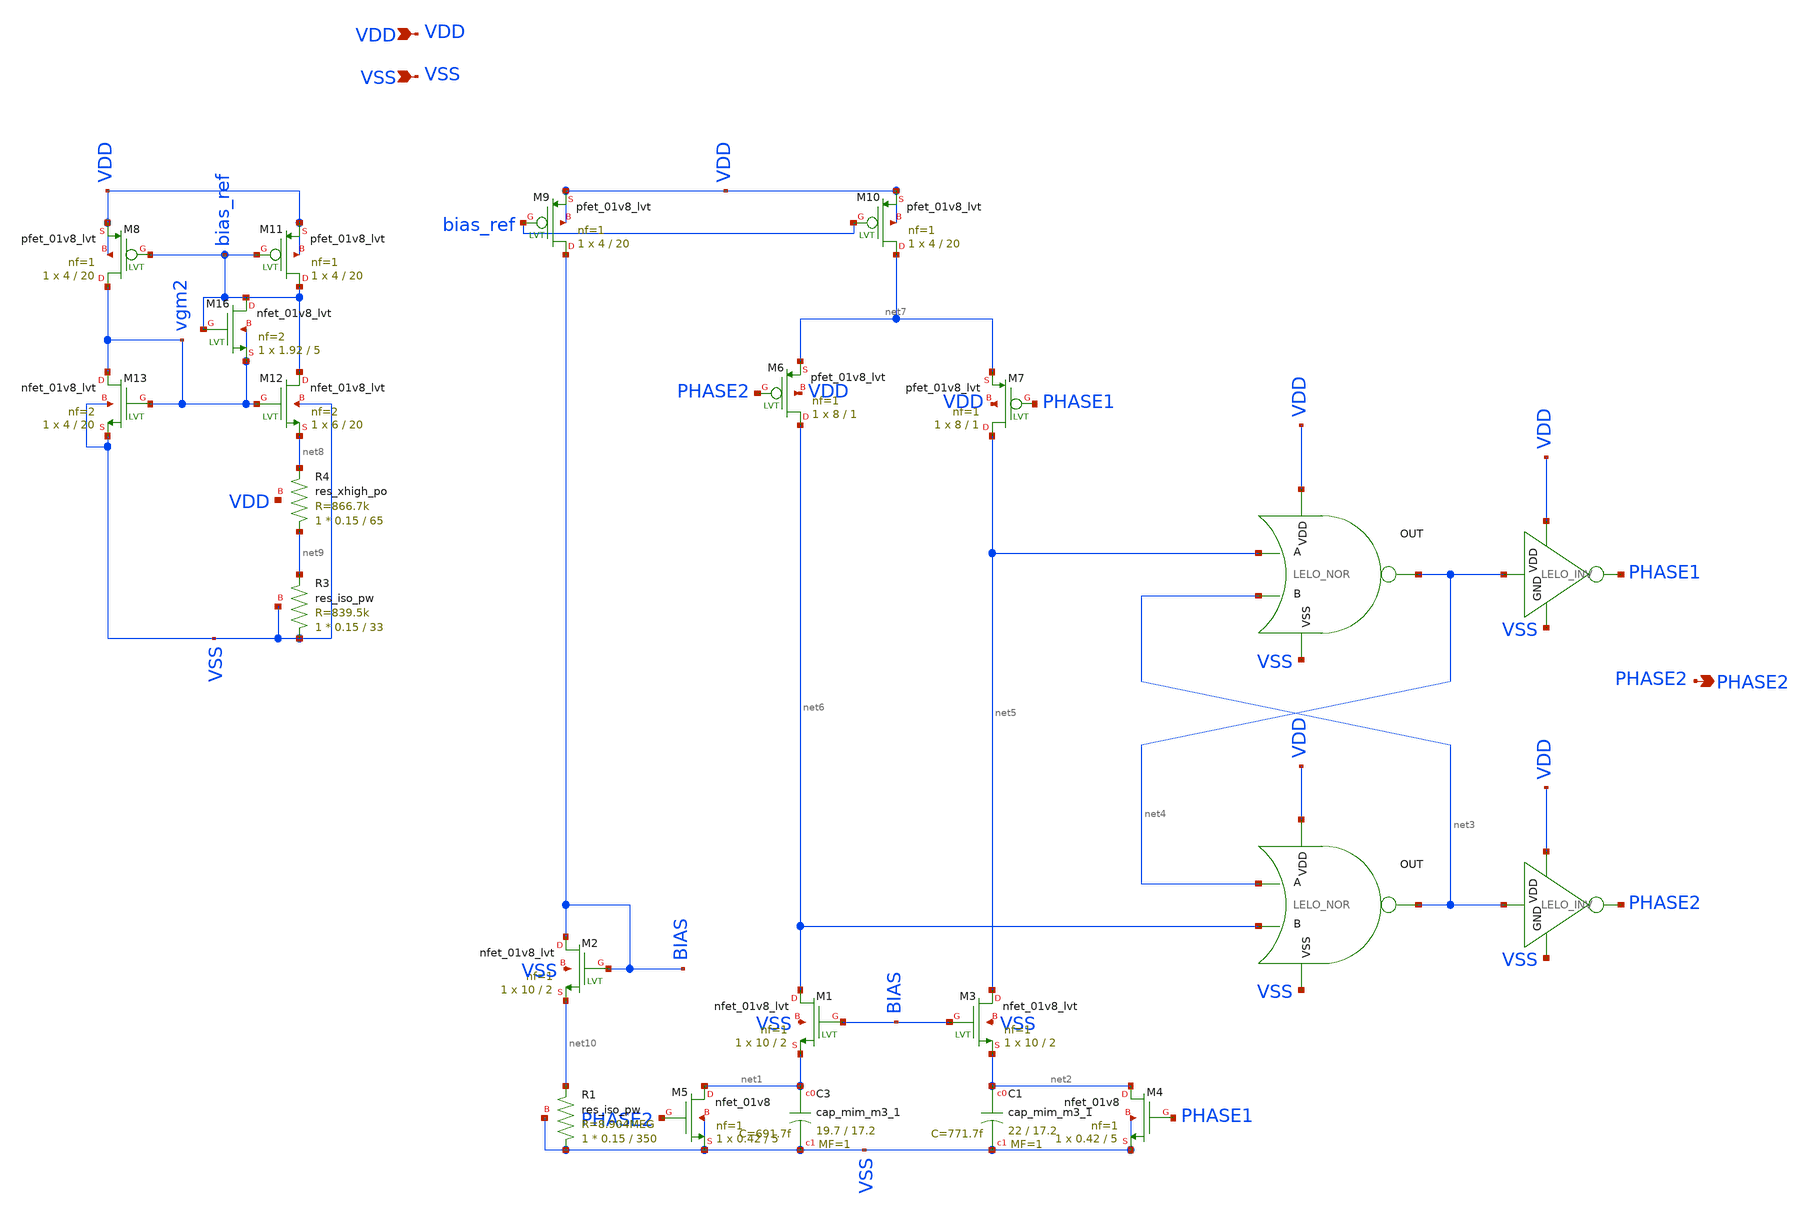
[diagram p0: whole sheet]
** sch_path: design/LELO_SVOD_SKY130A/LELO_SVOD_RELOSC.sch
**.subckt LELO_SVOD_RELOSC VDD VSS PHASE2
*.ipin VDD
*.ipin VSS
*.opin PHASE2
x1 VDD net4 net5 net3 VSS LELO_NOR
x2 VDD net3 net4 net6 VSS LELO_NOR
XM6 net6 PHASE2 net7 VDD sky130_fd_pr__pfet_01v8_lvt L=1 W=8 nf=1 ad='int((1 + 1)/2) * 8 / 1 * 0.29'
+ as='int((1 + 2)/2) * 8 / 1 * 0.29' pd='2*int((1 + 1)/2) * (8 / 1 + 0.29)' ps='2*int((1 + 2)/2) * (8 / 1 + 0.29)'
+ nrd='0.29 / 8 ' nrs='0.29 / 8 ' sa=0 sb=0 sd=0 mult=1 m=1
XM7 net5 PHASE1 net7 VDD sky130_fd_pr__pfet_01v8_lvt L=1 W=8 nf=1 ad='int((1 + 1)/2) * 8 / 1 * 0.29'
+ as='int((1 + 2)/2) * 8 / 1 * 0.29' pd='2*int((1 + 1)/2) * (8 / 1 + 0.29)' ps='2*int((1 + 2)/2) * (8 / 1 + 0.29)'
+ nrd='0.29 / 8 ' nrs='0.29 / 8 ' sa=0 sb=0 sd=0 mult=1 m=1
x3 VDD net4 PHASE1 VSS LELO_INV
x4 VDD net3 PHASE2 VSS LELO_INV
XM11 bias_ref bias_ref VDD VDD sky130_fd_pr__pfet_01v8_lvt L=20 W=4 nf=1 ad='int((1 + 1)/2) * 4 / 1 * 0.29'
+ as='int((1 + 2)/2) * 4 / 1 * 0.29' pd='2*int((1 + 1)/2) * (4 / 1 + 0.29)' ps='2*int((1 + 2)/2) * (4 / 1 + 0.29)'
+ nrd='0.29 / 4 ' nrs='0.29 / 4 ' sa=0 sb=0 sd=0 mult=1 m=1
XM16 bias_ref bias_ref vgm2 vgm2 sky130_fd_pr__nfet_01v8_lvt L=5 W=1.92 nf=2 ad='int((2 + 1)/2) * 1.92 / 2 * 0.29'
+ as='int((2 + 2)/2) * 1.92 / 2 * 0.29' pd='2*int((2 + 1)/2) * (1.92 / 2 + 0.29)' ps='2*int((2 + 2)/2) * (1.92 / 2 + 0.29)'
+ nrd='0.29 / 1.92 ' nrs='0.29 / 1.92 ' sa=0 sb=0 sd=0 mult=1 m=1
XC3 net1 VSS sky130_fd_pr__cap_mim_m3_1 W=19.7 L=17.2 MF=1 m=1
XC1 net2 VSS sky130_fd_pr__cap_mim_m3_1 W=22 L=17.2 MF=1 m=1
XR3 VSS net9 VSS sky130_fd_pr__res_iso_pw W=0.15 L=33 m=1
XR1 VSS net10 VSS sky130_fd_pr__res_iso_pw W=0.15 L=350 m=1
XR4 net9 net8 VDD sky130_fd_pr__res_xhigh_po W=0.15 L=65 mult=1 m=1
XM2 BIAS BIAS net10 VSS sky130_fd_pr__nfet_01v8_lvt L=2 W=10 nf=1 ad='int((1 + 1)/2) * 10 / 1 * 0.29'
+ as='int((1 + 2)/2) * 10 / 1 * 0.29' pd='2*int((1 + 1)/2) * (10 / 1 + 0.29)' ps='2*int((1 + 2)/2) * (10 / 1 + 0.29)'
+ nrd='0.29 / 10 ' nrs='0.29 / 10 ' sa=0 sb=0 sd=0 mult=1 m=1
XM4 net2 PHASE1 VSS VSS sky130_fd_pr__nfet_01v8 L=5 W=0.42 nf=1 ad='int((1 + 1)/2) * 0.42 / 1 * 0.29'
+ as='int((1 + 2)/2) * 0.42 / 1 * 0.29' pd='2*int((1 + 1)/2) * (0.42 / 1 + 0.29)' ps='2*int((1 + 2)/2) * (0.42 / 1 + 0.29)'
+ nrd='0.29 / 0.42 ' nrs='0.29 / 0.42 ' sa=0 sb=0 sd=0 mult=1 m=1
XM5 net1 PHASE2 VSS VSS sky130_fd_pr__nfet_01v8 L=5 W=0.42 nf=1 ad='int((1 + 1)/2) * 0.42 / 1 * 0.29'
+ as='int((1 + 2)/2) * 0.42 / 1 * 0.29' pd='2*int((1 + 1)/2) * (0.42 / 1 + 0.29)' ps='2*int((1 + 2)/2) * (0.42 / 1 + 0.29)'
+ nrd='0.29 / 0.42 ' nrs='0.29 / 0.42 ' sa=0 sb=0 sd=0 mult=1 m=1
XM1 net6 BIAS net1 VSS sky130_fd_pr__nfet_01v8_lvt L=2 W=10 nf=1 ad='int((1 + 1)/2) * 10 / 1 * 0.29'
+ as='int((1 + 2)/2) * 10 / 1 * 0.29' pd='2*int((1 + 1)/2) * (10 / 1 + 0.29)' ps='2*int((1 + 2)/2) * (10 / 1 + 0.29)'
+ nrd='0.29 / 10 ' nrs='0.29 / 10 ' sa=0 sb=0 sd=0 mult=1 m=1
XM3 net5 BIAS net2 VSS sky130_fd_pr__nfet_01v8_lvt L=2 W=10 nf=1 ad='int((1 + 1)/2) * 10 / 1 * 0.29'
+ as='int((1 + 2)/2) * 10 / 1 * 0.29' pd='2*int((1 + 1)/2) * (10 / 1 + 0.29)' ps='2*int((1 + 2)/2) * (10 / 1 + 0.29)'
+ nrd='0.29 / 10 ' nrs='0.29 / 10 ' sa=0 sb=0 sd=0 mult=1 m=1
XM8 vgm2 bias_ref VDD VDD sky130_fd_pr__pfet_01v8_lvt L=20 W=4 nf=1 ad='int((1 + 1)/2) * 4 / 1 * 0.29'
+ as='int((1 + 2)/2) * 4 / 1 * 0.29' pd='2*int((1 + 1)/2) * (4 / 1 + 0.29)' ps='2*int((1 + 2)/2) * (4 / 1 + 0.29)'
+ nrd='0.29 / 4 ' nrs='0.29 / 4 ' sa=0 sb=0 sd=0 mult=1 m=1
XM12 bias_ref vgm2 net8 VSS sky130_fd_pr__nfet_01v8_lvt L=20 W=6 nf=2 ad='int((2 + 1)/2) * 6 / 2 * 0.29'
+ as='int((2 + 2)/2) * 6 / 2 * 0.29' pd='2*int((2 + 1)/2) * (6 / 2 + 0.29)' ps='2*int((2 + 2)/2) * (6 / 2 + 0.29)'
+ nrd='0.29 / 6 ' nrs='0.29 / 6 ' sa=0 sb=0 sd=0 mult=1 m=1
XM13 vgm2 vgm2 VSS VSS sky130_fd_pr__nfet_01v8_lvt L=20 W=4 nf=2 ad='int((2 + 1)/2) * 4 / 2 * 0.29' as='int((2 + 2)/2) * 4 / 2 * 0.29'
+ pd='2*int((2 + 1)/2) * (4 / 2 + 0.29)' ps='2*int((2 + 2)/2) * (4 / 2 + 0.29)' nrd='0.29 / 4 ' nrs='0.29 / 4 '
+ sa=0 sb=0 sd=0 mult=1 m=1
XM9 BIAS bias_ref VDD VDD sky130_fd_pr__pfet_01v8_lvt L=20 W=4 nf=1 ad='int((1 + 1)/2) * 4 / 1 * 0.29'
+ as='int((1 + 2)/2) * 4 / 1 * 0.29' pd='2*int((1 + 1)/2) * (4 / 1 + 0.29)' ps='2*int((1 + 2)/2) * (4 / 1 + 0.29)'
+ nrd='0.29 / 4 ' nrs='0.29 / 4 ' sa=0 sb=0 sd=0 mult=1 m=1
XM10 net7 bias_ref VDD VDD sky130_fd_pr__pfet_01v8_lvt L=20 W=4 nf=1 ad='int((1 + 1)/2) * 4 / 1 * 0.29'
+ as='int((1 + 2)/2) * 4 / 1 * 0.29' pd='2*int((1 + 1)/2) * (4 / 1 + 0.29)' ps='2*int((1 + 2)/2) * (4 / 1 + 0.29)'
+ nrd='0.29 / 4 ' nrs='0.29 / 4 ' sa=0 sb=0 sd=0 mult=1 m=1
**.ends

* expanding   symbol:  LELO_SVOD_SKY130A/LELO_NOR.sym # of pins=5
** sym_path: design/LELO_SVOD_SKY130A/LELO_NOR.sym
** sch_path: design/LELO_SVOD_SKY130A/LELO_NOR.sch
.subckt LELO_NOR VDD OUT A B VSS
*.ipin VDD
*.ipin VSS
*.opin OUT
*.ipin A
*.ipin B
XM2 OUT B VSS VSS sky130_fd_pr__nfet_01v8 L=0.15 W=2 nf=1 ad='int((1 + 1)/2) * 2 / 1 * 0.29' as='int((1 + 2)/2) * 2 / 1 * 0.29'
+ pd='2*int((1 + 1)/2) * (2 / 1 + 0.29)' ps='2*int((1 + 2)/2) * (2 / 1 + 0.29)' nrd='0.29 / 2 ' nrs='0.29 / 2 '
+ sa=0 sb=0 sd=0 mult=1 m=1
XM1 OUT A VSS VSS sky130_fd_pr__nfet_01v8 L=0.15 W=2 nf=1 ad='int((1 + 1)/2) * 2 / 1 * 0.29' as='int((1 + 2)/2) * 2 / 1 * 0.29'
+ pd='2*int((1 + 1)/2) * (2 / 1 + 0.29)' ps='2*int((1 + 2)/2) * (2 / 1 + 0.29)' nrd='0.29 / 2 ' nrs='0.29 / 2 '
+ sa=0 sb=0 sd=0 mult=1 m=1
XM3 OUT B net1 VDD sky130_fd_pr__pfet_01v8 L=0.15 W=4 nf=1 ad='int((1 + 1)/2) * 4 / 1 * 0.29' as='int((1 + 2)/2) * 4 / 1 * 0.29'
+ pd='2*int((1 + 1)/2) * (4 / 1 + 0.29)' ps='2*int((1 + 2)/2) * (4 / 1 + 0.29)' nrd='0.29 / 4 ' nrs='0.29 / 4 '
+ sa=0 sb=0 sd=0 mult=1 m=1
XM4 net1 A VDD VDD sky130_fd_pr__pfet_01v8 L=0.15 W=4 nf=1 ad='int((1 + 1)/2) * 4 / 1 * 0.29' as='int((1 + 2)/2) * 4 / 1 * 0.29'
+ pd='2*int((1 + 1)/2) * (4 / 1 + 0.29)' ps='2*int((1 + 2)/2) * (4 / 1 + 0.29)' nrd='0.29 / 4 ' nrs='0.29 / 4 '
+ sa=0 sb=0 sd=0 mult=1 m=1
.ends


* expanding   symbol:  LELO_SVOD_SKY130A/LELO_INV.sym # of pins=4
** sym_path: design/LELO_SVOD_SKY130A/LELO_INV.sym
** sch_path: design/LELO_SVOD_SKY130A/LELO_INV.sch
.subckt LELO_INV VDD VIN VOUT GND
*.ipin VIN
*.ipin VDD
*.ipin GND
*.opin VOUT
XM1 VOUT VIN GND GND sky130_fd_pr__nfet_01v8_lvt L=0.15 W=1 nf=1 ad='int((1 + 1)/2) * 1 / 1 * 0.29' as='int((1 + 2)/2) * 1 / 1 * 0.29'
+ pd='2*int((1 + 1)/2) * (1 / 1 + 0.29)' ps='2*int((1 + 2)/2) * (1 / 1 + 0.29)' nrd='0.29 / 1 ' nrs='0.29 / 1 '
+ sa=0 sb=0 sd=0 mult=1 m=1
XM2 VOUT VIN VDD VDD sky130_fd_pr__pfet_01v8_lvt L=0.35 W=1 nf=1 ad='int((1 + 1)/2) * 1 / 1 * 0.29' as='int((1 + 2)/2) * 1 / 1 * 0.29'
+ pd='2*int((1 + 1)/2) * (1 / 1 + 0.29)' ps='2*int((1 + 2)/2) * (1 / 1 + 0.29)' nrd='0.29 / 1 ' nrs='0.29 / 1 '
+ sa=0 sb=0 sd=0 mult=2 m=2
.ends

.end
